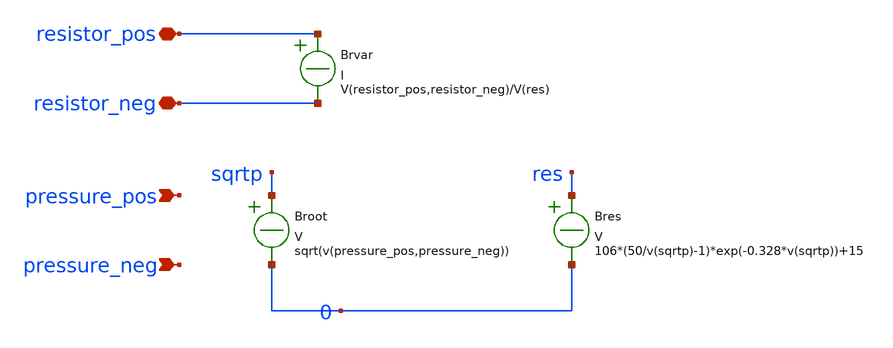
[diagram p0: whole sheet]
** sch_path: piezoresistor.sch
* Copyright 2020 Stefan Frederik Schippers
* Licensed under the Apache License, Version 2.0 (the "License");
* you may not use this file except in compliance with the License.
* You may obtain a copy of the License at
* https://www.apache.org/licenses/LICENSE-2.0
* Unless required by applicable law or agreed to in writing, software
* distributed under the License is distributed on an "AS IS" BASIS,
* WITHOUT WARRANTIES OR CONDITIONS OF ANY KIND, either express or implied.
* See the License for the specific language governing permissions and
* limitations under the License.
**.subckt piezoresistor pressure_pos pressure_neg resistor_pos resistor_neg
*.ipin pressure_pos
*.ipin pressure_neg
*.iopin resistor_pos
*.iopin resistor_neg
Broot sqrtp 0 V = sqrt(v(pressure_pos,pressure_neg))
Bres res 0 V = 106*(50/v(sqrtp)-1)*exp(-0.328*v(sqrtp))+15
Brvar resistor_pos resistor_neg I = V(resistor_pos,resistor_neg)/V(res)
**.ends
.end
